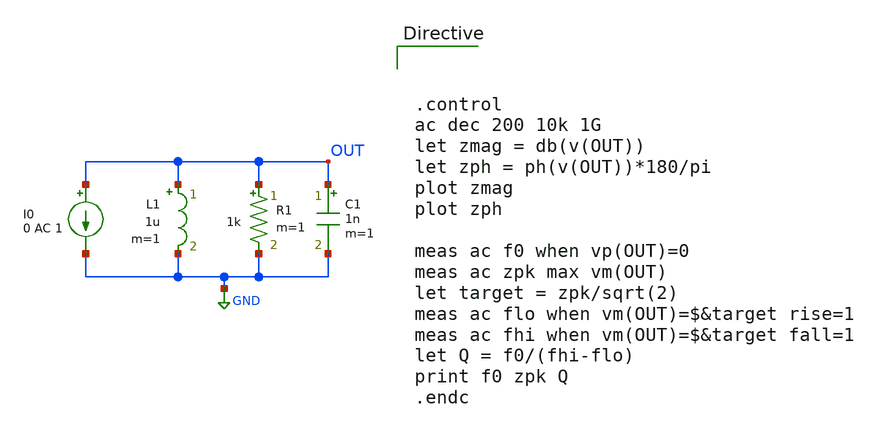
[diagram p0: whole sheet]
** sch_path: designs/sophiazhu/session_0/RLC_Tank.sch
**.subckt RLC_Tank
R1 OUT GND 1k m=1
C1 OUT GND 1n m=1
L1 OUT GND 1u m=1
I0 OUT GND 0 AC 1
**** begin user architecture code



.control
ac dec 200 10k 1G
let zmag = db(v(OUT))
let zph = ph(v(OUT))*180/pi
plot zmag
plot zph

meas ac f0 when vp(OUT)=0
meas ac zpk max vm(OUT)
let target = zpk/sqrt(2)
meas ac flo when vm(OUT)=$&target rise=1
meas ac fhi when vm(OUT)=$&target fall=1
let Q = f0/(fhi-flo)
print f0 zpk Q
.endc



**** end user architecture code
**.ends
.GLOBAL GND
.end
